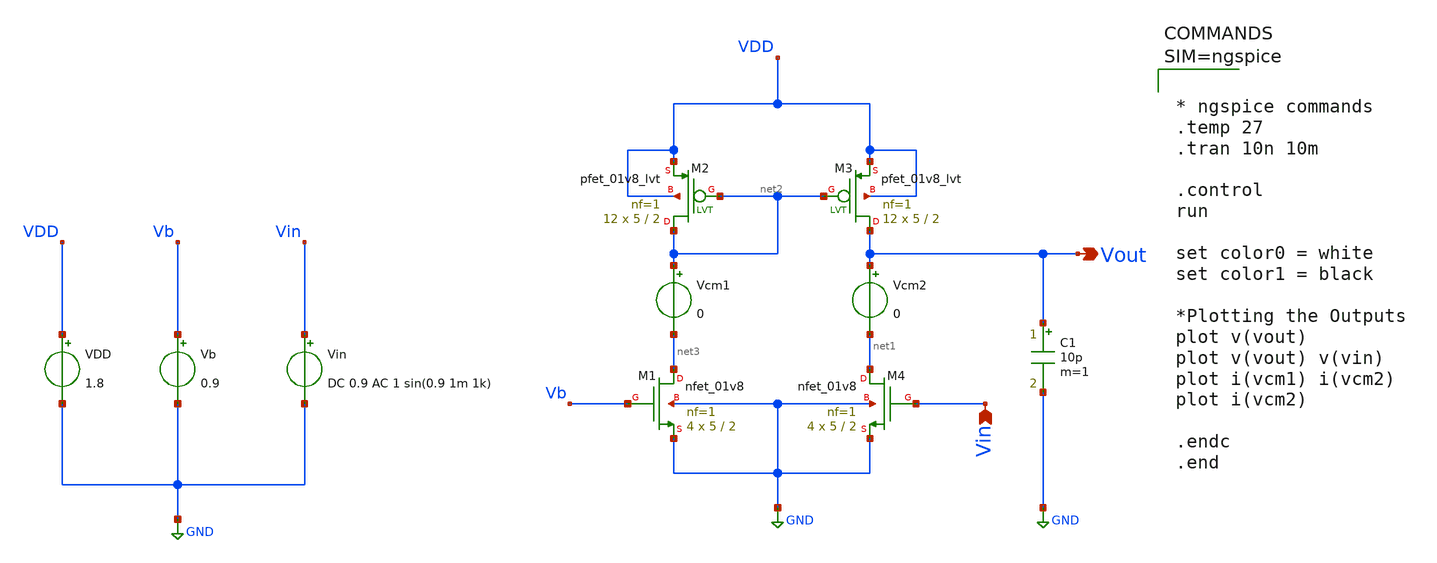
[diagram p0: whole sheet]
** sch_path: Common_Source_PMOS_Current_Source_Load_ckts/CS_Amp_PMOS_Current_Source_Load_AC_Transient_Analysis_ckt.sch
**.subckt CS_Amp_PMOS_Current_Source_Load_AC_Transient_Analysis_ckt Vout Vin
*.opin Vout
*.ipin Vin
XM1 net3 Vb GND GND sky130_fd_pr__nfet_01v8 L=2 W=5 nf=1 ad='int((1 + 1)/2) * 5 / 1 * 0.29' as='int((1 + 2)/2) * 5 / 1 * 0.29'
+ pd='2*int((1 + 1)/2) * (5 / 1 + 0.29)' ps='2*int((1 + 2)/2) * (5 / 1 + 0.29)' nrd='0.29 / 5 ' nrs='0.29 / 5 '
+ sa=0 sb=0 sd=0 mult=4 m=4
XM2 net2 net2 VDD VDD sky130_fd_pr__pfet_01v8_lvt L=2 W=5 nf=1 ad='int((1 + 1)/2) * 5 / 1 * 0.29' as='int((1 + 2)/2) * 5 / 1 * 0.29'
+ pd='2*int((1 + 1)/2) * (5 / 1 + 0.29)' ps='2*int((1 + 2)/2) * (5 / 1 + 0.29)' nrd='0.29 / 5 ' nrs='0.29 / 5 '
+ sa=0 sb=0 sd=0 mult=12 m=12
XM3 Vout net2 VDD VDD sky130_fd_pr__pfet_01v8_lvt L=2 W=5 nf=1 ad='int((1 + 1)/2) * 5 / 1 * 0.29' as='int((1 + 2)/2) * 5 / 1 * 0.29'
+ pd='2*int((1 + 1)/2) * (5 / 1 + 0.29)' ps='2*int((1 + 2)/2) * (5 / 1 + 0.29)' nrd='0.29 / 5 ' nrs='0.29 / 5 '
+ sa=0 sb=0 sd=0 mult=12 m=12
XM4 net1 Vin GND GND sky130_fd_pr__nfet_01v8 L=2 W=5 nf=1 ad='int((1 + 1)/2) * 5 / 1 * 0.29' as='int((1 + 2)/2) * 5 / 1 * 0.29'
+ pd='2*int((1 + 1)/2) * (5 / 1 + 0.29)' ps='2*int((1 + 2)/2) * (5 / 1 + 0.29)' nrd='0.29 / 5 ' nrs='0.29 / 5 '
+ sa=0 sb=0 sd=0 mult=4 m=4
Vb Vb GND 0.9
Vin Vin GND DC 0.9 AC 1 sin(0.9 1m 1k)
VDD VDD GND 1.8
Vcm1 net2 net3 0
Vcm2 Vout net1 0
C1 Vout GND 10p m=1
**** begin user architecture code



* ngspice commands
.temp 27
.tran 10n 10m

.control
run

set color0 = white
set color1 = black

*Plotting the Outputs
plot v(vout)
plot v(vout) v(vin)
plot i(vcm1) i(vcm2)
plot i(vcm2)

.endc
.end






** opencircuitdesign pdks install
.lib $::SKYWATER_MODELS/sky130.lib.spice tt

**** end user architecture code
**.ends
.GLOBAL GND
.end
